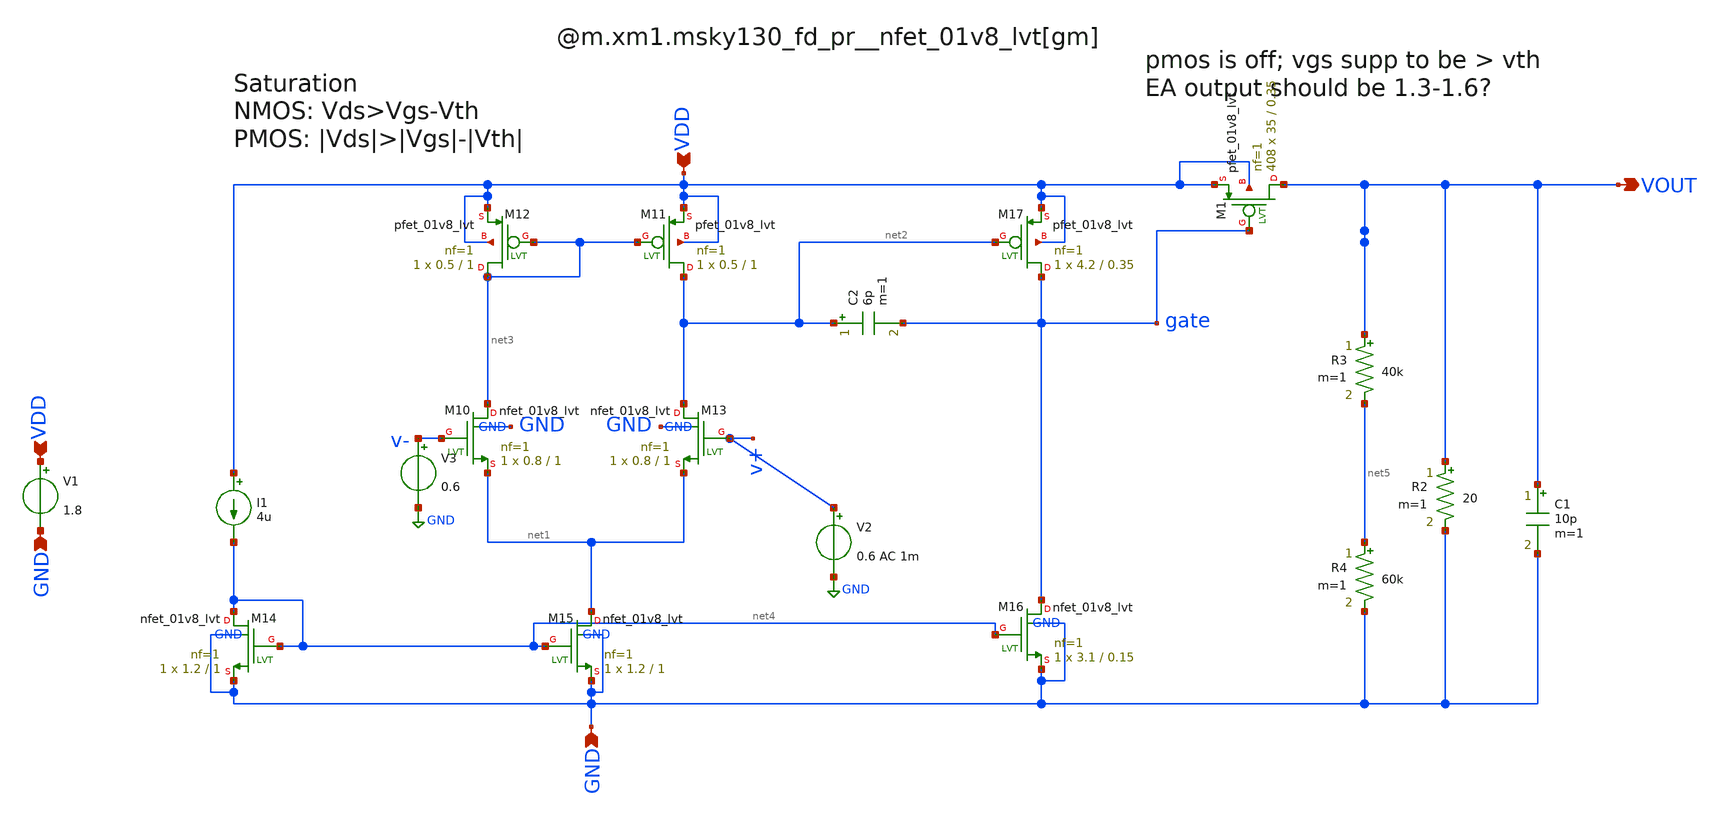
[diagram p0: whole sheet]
** sch_path: xschem/testbenches/FreqResponse-v3.sch
**.subckt FreqResponse-v3 VDD VOUT GND VDD GND
*.ipin VDD
*.opin VOUT
*.ipin GND
*.ipin VDD
*.ipin GND
C2 net2 gate 6p m=1
I1 VDD net4 4u
V3 v- GND 0.6
XM10 net3 v- net1 GND sky130_fd_pr__nfet_01v8_lvt L=1 W=0.8 nf=1 ad='int((1 + 1)/2) * 0.8 / 1 * 0.29'
+ as='int((1 + 2)/2) * 0.8 / 1 * 0.29' pd='2*int((1 + 1)/2) * (0.8 / 1 + 0.29)' ps='2*int((1 + 2)/2) * (0.8 / 1 + 0.29)'
+ nrd='0.29 / 0.8 ' nrs='0.29 / 0.8 ' sa=0 sb=0 sd=0 mult=1 m=1
XM11 net2 net3 VDD VDD sky130_fd_pr__pfet_01v8_lvt L=1 W=0.5 nf=1 ad='int((1 + 1)/2) * 0.5 / 1 * 0.29'
+ as='int((1 + 2)/2) * 0.5 / 1 * 0.29' pd='2*int((1 + 1)/2) * (0.5 / 1 + 0.29)' ps='2*int((1 + 2)/2) * (0.5 / 1 + 0.29)'
+ nrd='0.29 / 0.5 ' nrs='0.29 / 0.5 ' sa=0 sb=0 sd=0 mult=1 m=1
XM12 net3 net3 VDD VDD sky130_fd_pr__pfet_01v8_lvt L=1 W=0.5 nf=1 ad='int((1 + 1)/2) * 0.5 / 1 * 0.29'
+ as='int((1 + 2)/2) * 0.5 / 1 * 0.29' pd='2*int((1 + 1)/2) * (0.5 / 1 + 0.29)' ps='2*int((1 + 2)/2) * (0.5 / 1 + 0.29)'
+ nrd='0.29 / 0.5 ' nrs='0.29 / 0.5 ' sa=0 sb=0 sd=0 mult=1 m=1
XM13 net2 v+ net1 GND sky130_fd_pr__nfet_01v8_lvt L=1 W=0.8 nf=1 ad='int((1 + 1)/2) * 0.8 / 1 * 0.29'
+ as='int((1 + 2)/2) * 0.8 / 1 * 0.29' pd='2*int((1 + 1)/2) * (0.8 / 1 + 0.29)' ps='2*int((1 + 2)/2) * (0.8 / 1 + 0.29)'
+ nrd='0.29 / 0.8 ' nrs='0.29 / 0.8 ' sa=0 sb=0 sd=0 mult=1 m=1
XM14 net4 net4 GND GND sky130_fd_pr__nfet_01v8_lvt L=1 W=1.2 nf=1 ad='int((1 + 1)/2) * 1.2 / 1 * 0.29'
+ as='int((1 + 2)/2) * 1.2 / 1 * 0.29' pd='2*int((1 + 1)/2) * (1.2 / 1 + 0.29)' ps='2*int((1 + 2)/2) * (1.2 / 1 + 0.29)'
+ nrd='0.29 / 1.2 ' nrs='0.29 / 1.2 ' sa=0 sb=0 sd=0 mult=1 m=1
XM15 net1 net4 GND GND sky130_fd_pr__nfet_01v8_lvt L=1 W=1.2 nf=1 ad='int((1 + 1)/2) * 1.2 / 1 * 0.29'
+ as='int((1 + 2)/2) * 1.2 / 1 * 0.29' pd='2*int((1 + 1)/2) * (1.2 / 1 + 0.29)' ps='2*int((1 + 2)/2) * (1.2 / 1 + 0.29)'
+ nrd='0.29 / 1.2 ' nrs='0.29 / 1.2 ' sa=0 sb=0 sd=0 mult=1 m=1
XM16 gate net4 GND GND sky130_fd_pr__nfet_01v8_lvt L=0.15 W=3.1 nf=1 ad='int((1 + 1)/2) * 3.1 / 1 * 0.29'
+ as='int((1 + 2)/2) * 3.1 / 1 * 0.29' pd='2*int((1 + 1)/2) * (3.1 / 1 + 0.29)' ps='2*int((1 + 2)/2) * (3.1 / 1 + 0.29)'
+ nrd='0.29 / 3.1 ' nrs='0.29 / 3.1 ' sa=0 sb=0 sd=0 mult=1 m=1
XM17 gate net2 VDD VDD sky130_fd_pr__pfet_01v8_lvt L=0.35 W=4.2 nf=1 ad='int((1 + 1)/2) * 4.2 / 1 * 0.29'
+ as='int((1 + 2)/2) * 4.2 / 1 * 0.29' pd='2*int((1 + 1)/2) * (4.2 / 1 + 0.29)' ps='2*int((1 + 2)/2) * (4.2 / 1 + 0.29)'
+ nrd='0.29 / 4.2 ' nrs='0.29 / 4.2 ' sa=0 sb=0 sd=0 mult=1 m=1
R3 VOUT net5 40k m=1
R4 net5 GND 60k m=1
XM1 VOUT gate VDD VDD sky130_fd_pr__pfet_01v8_lvt L=0.35 W=35 nf=1 ad='int((1 + 1)/2) * 35 / 1 * 0.29'
+ as='int((1 + 2)/2) * 35 / 1 * 0.29' pd='2*int((1 + 1)/2) * (35 / 1 + 0.29)' ps='2*int((1 + 2)/2) * (35 / 1 + 0.29)'
+ nrd='0.29 / 35 ' nrs='0.29 / 35 ' sa=0 sb=0 sd=0 mult=408 m=408
V1 VDD GND 1.8
V2 v+ GND 0.6 AC 1m
R2 VOUT GND 20 m=1
C1 VOUT GND 10p m=1
**** begin user architecture code



.lib /usr/local/share/pdk/sky130A/libs.tech/ngspice/sky130.lib.spice tt
.ac dec 20 1 1e12
*.tran 5u 5m

.control
run
print 1/@m.xm1.msky130_fd_pr__pfet_01v8_lvt[gds]
*plot vout
plot db(vout/v(v+)) title c=100n
plot 180*cph(vout)/pi
.endc


**** end user architecture code
**.ends
.GLOBAL GND
.end
